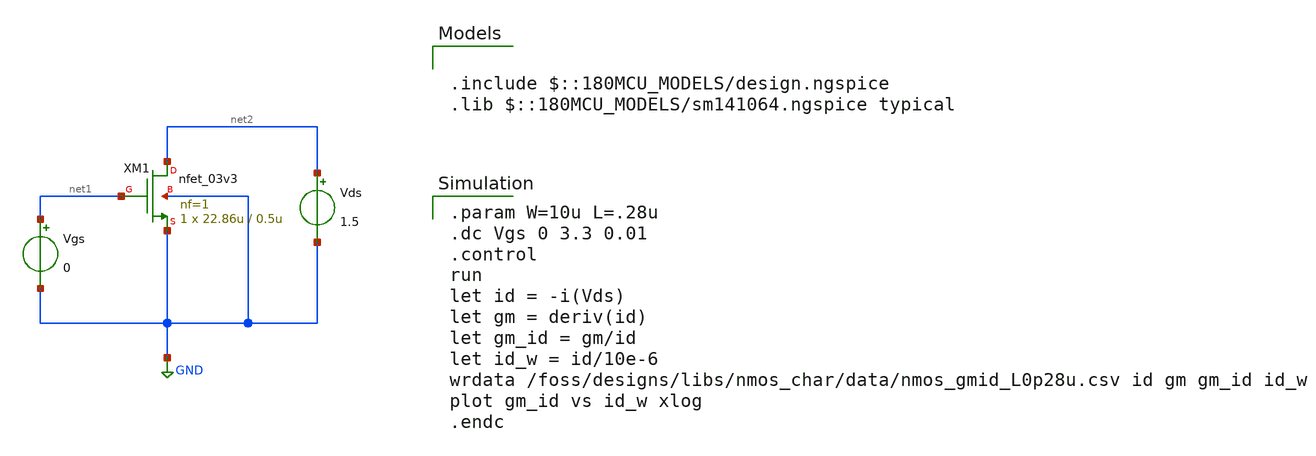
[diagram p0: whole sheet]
** sch_path: designs/libs/nmos_char/local_nmos_characterization.sch
**.subckt local_nmos_characterization
Vds net2 GND 1.5
Vgs net1 GND 0
XM1 net2 net1 GND GND nfet_03v3 L=0.5u W=22.86u nf=1 ad='int((nf+1)/2) * W/nf * 0.18u' as='int((nf+2)/2) * W/nf * 0.18u'
+ pd='2*int((nf+1)/2) * (W/nf + 0.18u)' ps='2*int((nf+2)/2) * (W/nf + 0.18u)' nrd='0.18u / W' nrs='0.18u / W'
+ sa=0 sb=0 sd=0 m=1
**** begin user architecture code

.param W=10u L=.28u
.dc Vgs 0 3.3 0.01
.control
run
let id = -i(Vds)
let gm = deriv(id)
let gm_id = gm/id
let id_w = id/10e-6
wrdata /foss/designs/libs/nmos_char/data/nmos_gmid_L0p28u.csv id gm gm_id id_w
plot gm_id vs id_w xlog
.endc


.include $::180MCU_MODELS/design.ngspice
.lib $::180MCU_MODELS/sm141064.ngspice typical

**** end user architecture code
**.ends
.GLOBAL GND
.end
